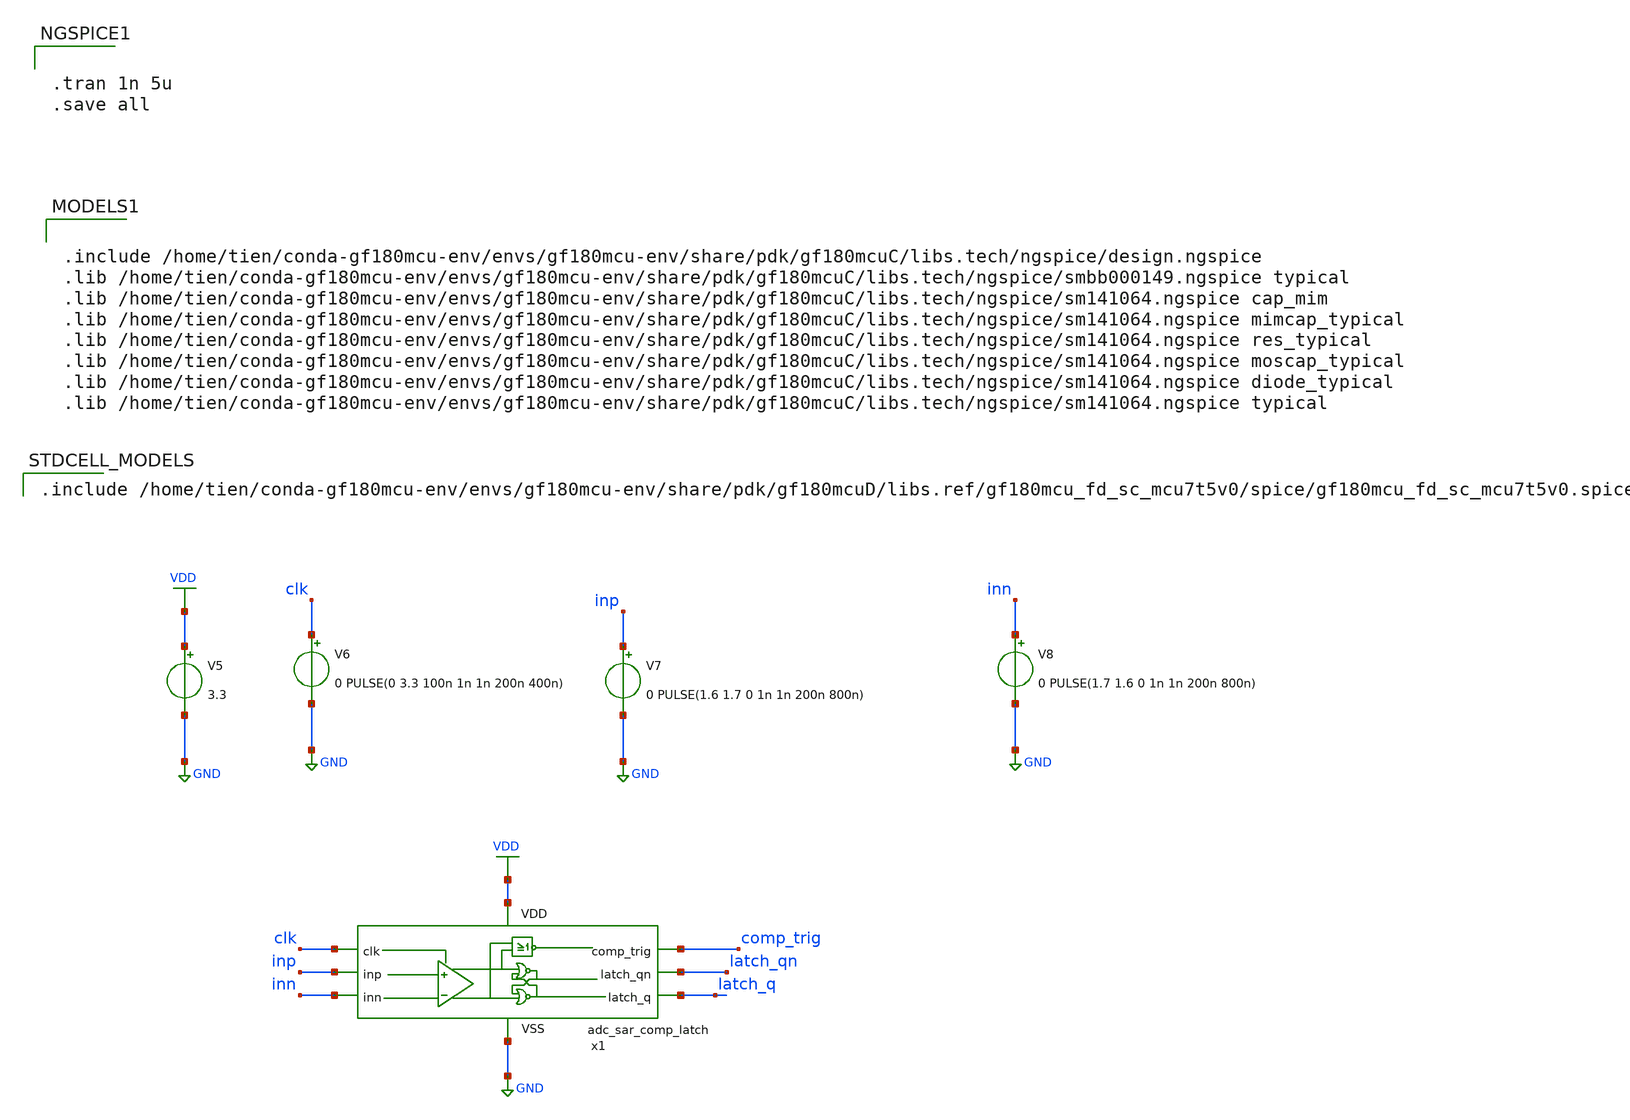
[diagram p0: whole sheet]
** sch_path: spice/adc_sar_comp_latch_tb.sch
**.subckt adc_sar_comp_latch_tb
V5 VDD GND 3.3
V6 clk GND 0 PULSE(0 3.3 100n 1n 1n 200n 400n)
V7 inp GND 0 PULSE(1.6 1.7 0 1n 1n 200n 800n)
V8 inn GND 0 PULSE(1.7 1.6 0 1n 1n 200n 800n)
x1 VDD GND clk inp inn comp_trig latch_qn latch_q adc_sar_comp_latch
**** begin user architecture code


.tran 1n 5u
.save all



.include /home/tien/conda-gf180mcu-env/envs/gf180mcu-env/share/pdk/gf180mcuC/libs.tech/ngspice/design.ngspice
.lib /home/tien/conda-gf180mcu-env/envs/gf180mcu-env/share/pdk/gf180mcuC/libs.tech/ngspice/smbb000149.ngspice typical
.lib /home/tien/conda-gf180mcu-env/envs/gf180mcu-env/share/pdk/gf180mcuC/libs.tech/ngspice/sm141064.ngspice cap_mim
.lib /home/tien/conda-gf180mcu-env/envs/gf180mcu-env/share/pdk/gf180mcuC/libs.tech/ngspice/sm141064.ngspice mimcap_typical
.lib /home/tien/conda-gf180mcu-env/envs/gf180mcu-env/share/pdk/gf180mcuC/libs.tech/ngspice/sm141064.ngspice res_typical
.lib /home/tien/conda-gf180mcu-env/envs/gf180mcu-env/share/pdk/gf180mcuC/libs.tech/ngspice/sm141064.ngspice moscap_typical
.lib /home/tien/conda-gf180mcu-env/envs/gf180mcu-env/share/pdk/gf180mcuC/libs.tech/ngspice/sm141064.ngspice diode_typical
.lib /home/tien/conda-gf180mcu-env/envs/gf180mcu-env/share/pdk/gf180mcuC/libs.tech/ngspice/sm141064.ngspice typical

 .include /home/tien/conda-gf180mcu-env/envs/gf180mcu-env/share/pdk/gf180mcuD/libs.ref/gf180mcu_fd_sc_mcu7t5v0/spice/gf180mcu_fd_sc_mcu7t5v0.spice
**** end user architecture code
**.ends
.GLOBAL GND
.GLOBAL VDD
.end
